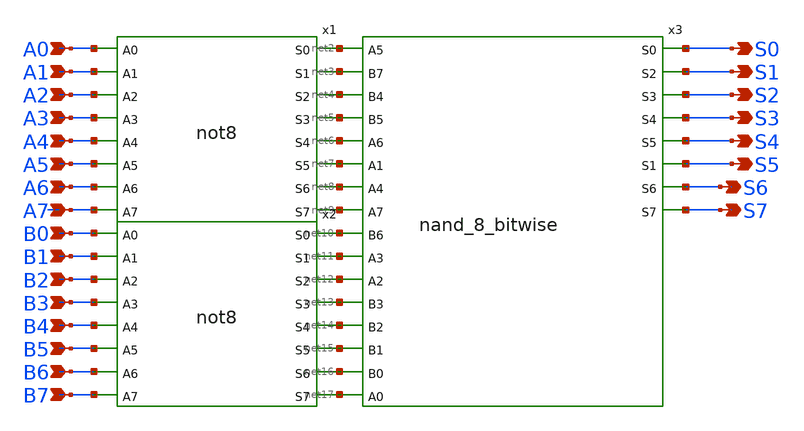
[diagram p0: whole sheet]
** sch_path: design/xschem/OR/OR8.sch
**.subckt OR8 A0 A1 B1 A2 B2 A3 B3 A4 B4 A5 B5 A6 B6 A7 B7 B0 S6 S7 S3 S4 S5 S0 S1 S2
*.ipin A0
*.ipin A1
*.ipin B1
*.ipin A2
*.ipin B2
*.ipin A3
*.ipin B3
*.ipin A4
*.ipin B4
*.ipin A5
*.ipin B5
*.ipin A6
*.ipin B6
*.ipin A7
*.ipin B7
*.ipin B0
*.opin S6
*.opin S7
*.opin S3
*.opin S4
*.opin S5
*.opin S0
*.opin S1
*.opin S2
x1 A0 A1 A2 A3 A4 A5 A6 A7 net2 net3 net4 net5 net6 net7 net8 net9 not8
x2 B0 B1 B2 B3 B4 B5 B6 B7 net10 net11 net12 net13 net14 net15 net16 net17 not8
x3 net2 net3 net4 net5 net6 net7 net8 net9 net10 net11 net12 net13 net14 net15 net16 net17 S0 S1 S2
+ S3 S4 S5 S6 S7 nand_8_bitwise
**.ends
.end
